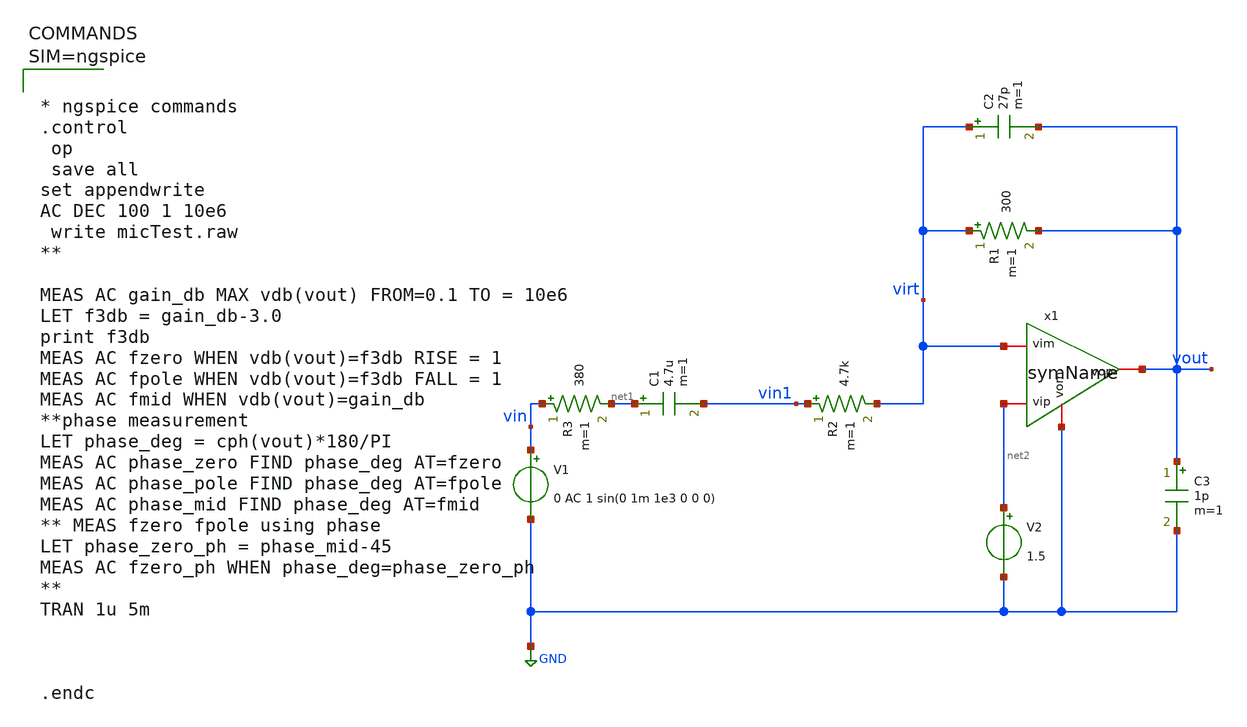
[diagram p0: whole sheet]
** sch_path: xschem/micTest.sch
**.subckt micTest
V1 vin GND 0 AC 1 sin(0 1m 1e3 0 0 0)
C1 net1 vin1 4.7u m=1
R2 vin1 virt 4.7k m=1
R1 virt vout 300 m=1
V2 net2 GND 1.5
R3 vin net1 380 m=1
C2 virt vout 27p m=1
C3 vout GND 1p m=1
x1 vout net2 virt GND symName
**** begin user architecture code



* ngspice commands
.control
 op
 save all
set appendwrite
AC DEC 100 1 10e6
 write micTest.raw
**

MEAS AC gain_db MAX vdb(vout) FROM=0.1 TO = 10e6
LET f3db = gain_db-3.0
print f3db
MEAS AC fzero WHEN vdb(vout)=f3db RISE = 1
MEAS AC fpole WHEN vdb(vout)=f3db FALL = 1
MEAS AC fmid WHEN vdb(vout)=gain_db
**phase measurement
LET phase_deg = cph(vout)*180/PI
MEAS AC phase_zero FIND phase_deg AT=fzero
MEAS AC phase_pole FIND phase_deg AT=fpole
MEAS AC phase_mid FIND phase_deg AT=fmid
** MEAS fzero fpole using phase
LET phase_zero_ph = phase_mid-45
MEAS AC fzero_ph WHEN phase_deg=phase_zero_ph
**
TRAN 1u 5m



.endc



**** end user architecture code
**.ends

* expanding   symbol:  symName.sym # of pins=4
** sym_path: xschem/symName.sym
** sch_path: xschem/symName.sch
.subckt symName vop vip vim vom
*.iopin vop
*.iopin vom
*.iopin vip
*.iopin vim
E1 vop vom vip vim 1000
.ends

.GLOBAL GND
.end
